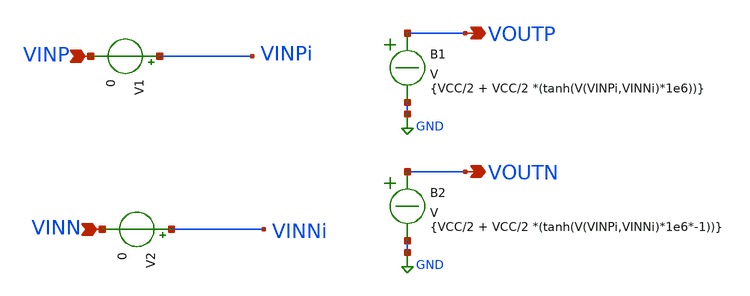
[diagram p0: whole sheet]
** sch_path: XSCHEM Files/comperator.sch
**.subckt comperator VINP VOUTP VINN VOUTN
*.ipin VINP
*.opin VOUTP
*.ipin VINN
*.opin VOUTN
V1 VINPi VINP 0
V2 VINNi VINN 0
B2 VOUTN GND V = {VCC/2 + VCC/2 *(tanh(V(VINPi,VINNi)*1e6*-1))}
B1 VOUTP GND V = {VCC/2 + VCC/2 *(tanh(V(VINPi,VINNi)*1e6))}
**.ends
.GLOBAL GND
.end
